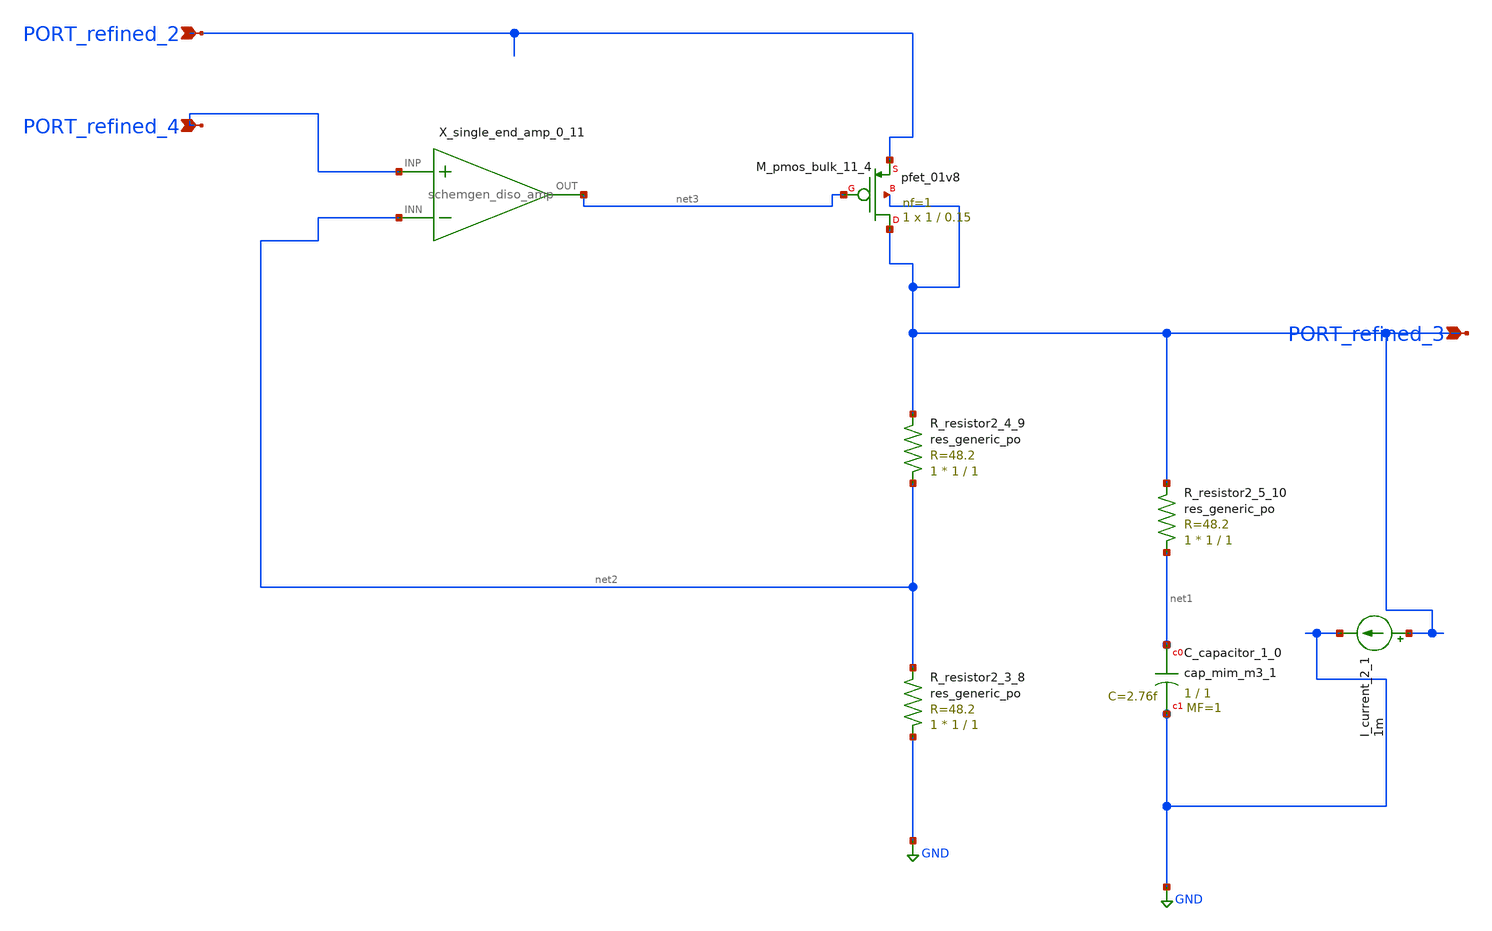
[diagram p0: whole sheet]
** sch_path: schematics/Image2Net/107.sch
**.subckt 107 PORT_refined_2 PORT_refined_3 PORT_refined_4
*.ipin PORT_refined_2
*.ipin PORT_refined_3
*.ipin PORT_refined_4
XC_capacitor_1_0 net1 GND sky130_fd_pr__cap_mim_m3_1 W=1 L=1 MF=1 m=1
I_current_2_1 PORT_refined_3 GND 1m
XM_pmos_bulk_11_4 PORT_refined_3 net3 PORT_refined_2 PORT_refined_3 sky130_fd_pr__pfet_01v8 L=0.15 W=1
+ nf=1 ad='int((1 + 1)/2) * 1 / 1 * 0.29' as='int((1 + 2)/2) * 1 / 1 * 0.29' pd='2*int((1 + 1)/2) * (1 / 1 + 0.29)'
+ ps='2*int((1 + 2)/2) * (1 / 1 + 0.29)' nrd='0.29 / 1 ' nrs='0.29 / 1 ' sa=0 sb=0 sd=0 mult=1 m=1
XR_resistor2_3_8 GND net2 sky130_fd_pr__res_generic_po W=1 L=1 m=1
XR_resistor2_4_9 net2 PORT_refined_3 sky130_fd_pr__res_generic_po W=1 L=1 m=1
XR_resistor2_5_10 net1 PORT_refined_3 sky130_fd_pr__res_generic_po W=1 L=1 m=1
X_single_end_amp_0_11 PORT_refined_4 net2 net3 schemgen_diso_amp
**.ends

* expanding   symbol:  schemgen_diso_amp.sym # of pins=3
** sym_path: symbols/schemgen_diso_amp.sym
.subckt schemgen_diso_amp INP INN OUT
* SchemGen ideal op-amp: Vout = 1e5 * (V(INP) - V(INN))
E1 OUT 0 INP INN 1e5
.ends schemgen_diso_amp
.GLOBAL GND
.end
